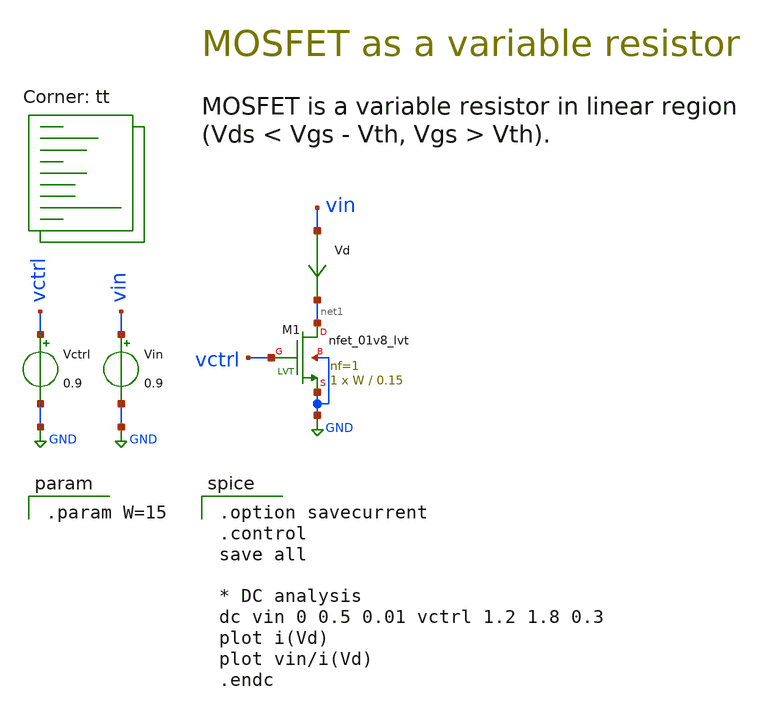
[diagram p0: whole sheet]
** sch_path: 00-c_variable-R.sch
**.subckt 00-c_variable-R
XM1 net1 vctrl GND GND sky130_fd_pr__nfet_01v8_lvt L=0.15 W=W nf=1 ad='int((1 + 1)/2) * W / 1 * 0.29'
+ as='int((1 + 2)/2) * W / 1 * 0.29' pd='2*int((1 + 1)/2) * (W / 1 + 0.29)' ps='2*int((1 + 2)/2) * (W / 1 + 0.29)'
+ nrd='0.29 / W ' nrs='0.29 / W ' sa=0 sb=0 sd=0 mult=1 m=1
Vctrl vctrl GND 0.9
Vin vin GND 0.9
Vd vin net1 0
.save i(vd)
**** begin user architecture code
.lib $::SKYWATER_MODELS/sky130.lib.spice tt

.param W=15


.option savecurrent
.control
save all

* DC analysis
dc vin 0 0.5 0.01 vctrl 1.2 1.8 0.3
plot i(Vd)
plot vin/i(Vd)
.endc

**** end user architecture code
**.ends
.GLOBAL GND
.end
